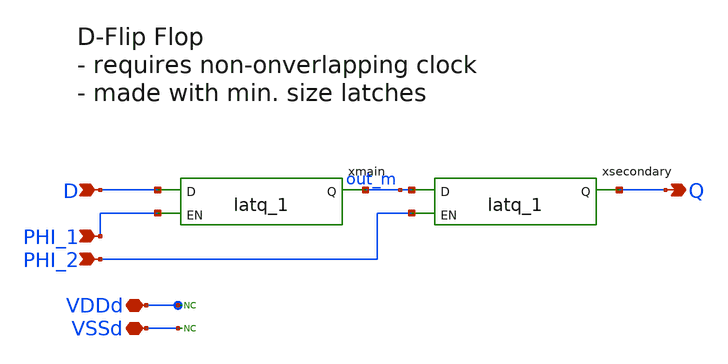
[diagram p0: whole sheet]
** sch_path: designs/switch_matrix_gf180mcu_9t5v0-main/DFF_2phase_1/DFF_2phase_1.sch
**.subckt DFF_2phase_1 D PHI_1 PHI_2 Q VDDd VSSd
*.ipin D
*.ipin PHI_1
*.ipin PHI_2
*.opin Q
*.iopin VDDd
*.iopin VSSd
xmain D PHI_1 out_m VDDd VDDd VSSd VSSd gf180mcu_fd_sc_mcu9t5v0__latq_1
xsecondary out_m PHI_2 Q VDDd VDDd VSSd VSSd gf180mcu_fd_sc_mcu9t5v0__latq_1
* noconn VSSd
* noconn VDDd
**.ends
.end
